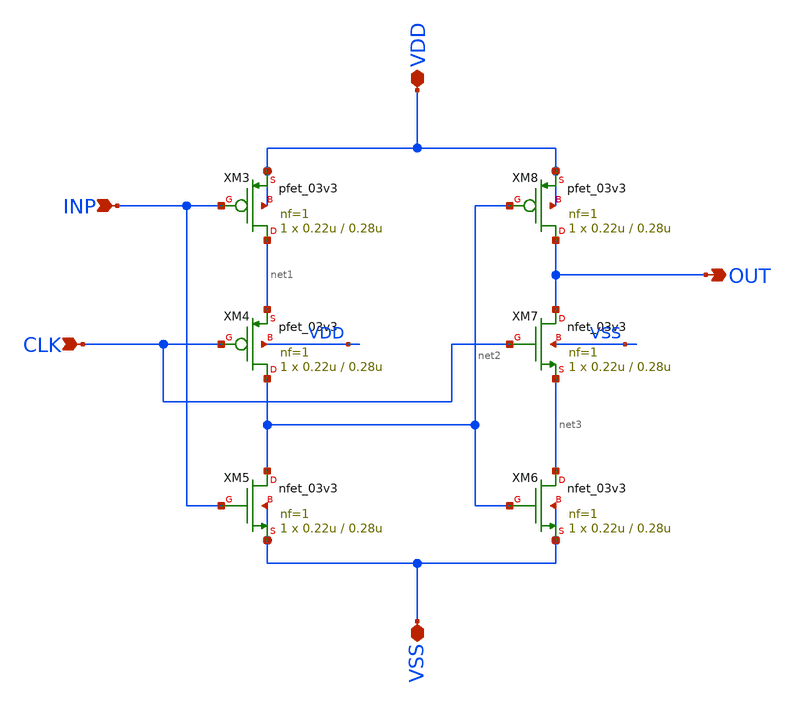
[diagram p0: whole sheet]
** sch_path: Clock_Generator_PAKISTAN_06/Schematics/HT_register.sch
**.subckt HT_register VSS VDD OUT INP CLK
*.iopin VSS
*.iopin VDD
*.opin OUT
*.ipin INP
*.ipin CLK
XM3 net1 INP VDD VDD pfet_03v3 L=0.28u W=0.22u nf=1 ad='int((nf+1)/2) * W/nf * 0.18u' as='int((nf+2)/2) * W/nf * 0.18u'
+ pd='2*int((nf+1)/2) * (W/nf + 0.18u)' ps='2*int((nf+2)/2) * (W/nf + 0.18u)' nrd='0.18u / W' nrs='0.18u / W'
+ sa=0 sb=0 sd=0 m=1
XM4 net2 CLK net1 VDD pfet_03v3 L=0.28u W=0.22u nf=1 ad='int((nf+1)/2) * W/nf * 0.18u' as='int((nf+2)/2) * W/nf * 0.18u'
+ pd='2*int((nf+1)/2) * (W/nf + 0.18u)' ps='2*int((nf+2)/2) * (W/nf + 0.18u)' nrd='0.18u / W' nrs='0.18u / W'
+ sa=0 sb=0 sd=0 m=1
XM5 net2 INP VSS VSS nfet_03v3 L=0.28u W=0.22u nf=1 ad='int((nf+1)/2) * W/nf * 0.18u' as='int((nf+2)/2) * W/nf * 0.18u'
+ pd='2*int((nf+1)/2) * (W/nf + 0.18u)' ps='2*int((nf+2)/2) * (W/nf + 0.18u)' nrd='0.18u / W' nrs='0.18u / W'
+ sa=0 sb=0 sd=0 m=1
XM6 net3 net2 VSS VSS nfet_03v3 L=0.28u W=0.22u nf=1 ad='int((nf+1)/2) * W/nf * 0.18u' as='int((nf+2)/2) * W/nf * 0.18u'
+ pd='2*int((nf+1)/2) * (W/nf + 0.18u)' ps='2*int((nf+2)/2) * (W/nf + 0.18u)' nrd='0.18u / W' nrs='0.18u / W'
+ sa=0 sb=0 sd=0 m=1
XM7 OUT CLK net3 VSS nfet_03v3 L=0.28u W=0.22u nf=1 ad='int((nf+1)/2) * W/nf * 0.18u' as='int((nf+2)/2) * W/nf * 0.18u'
+ pd='2*int((nf+1)/2) * (W/nf + 0.18u)' ps='2*int((nf+2)/2) * (W/nf + 0.18u)' nrd='0.18u / W' nrs='0.18u / W'
+ sa=0 sb=0 sd=0 m=1
XM8 OUT net2 VDD VDD pfet_03v3 L=0.28u W=0.22u nf=1 ad='int((nf+1)/2) * W/nf * 0.18u' as='int((nf+2)/2) * W/nf * 0.18u'
+ pd='2*int((nf+1)/2) * (W/nf + 0.18u)' ps='2*int((nf+2)/2) * (W/nf + 0.18u)' nrd='0.18u / W' nrs='0.18u / W'
+ sa=0 sb=0 sd=0 m=1
**.ends
.end
